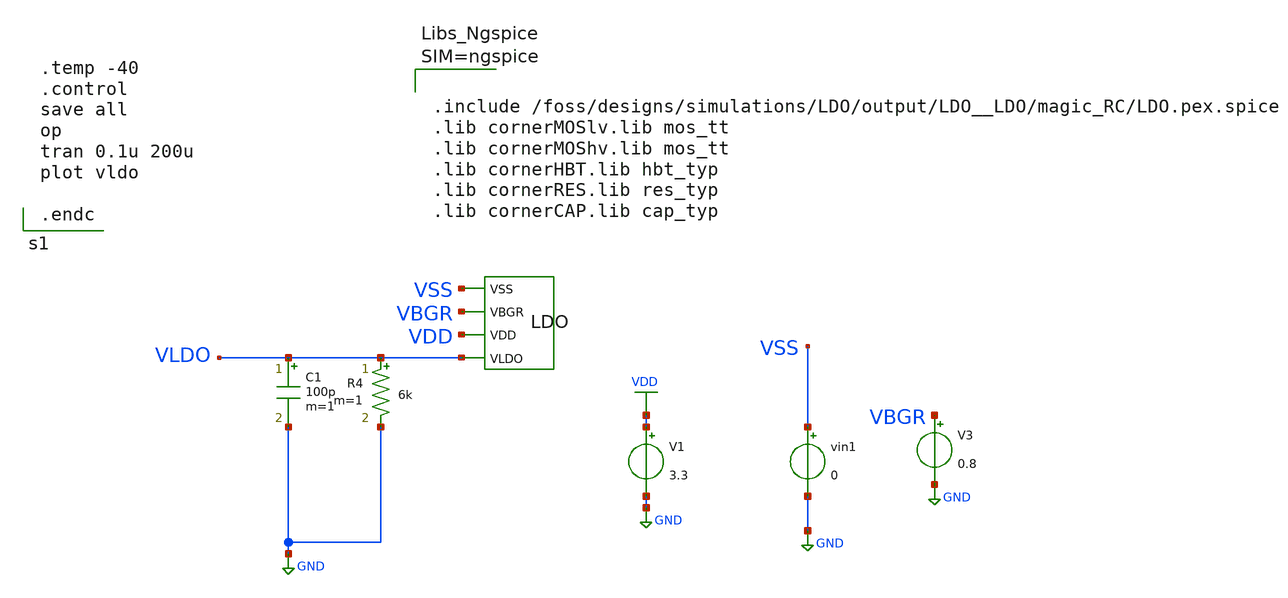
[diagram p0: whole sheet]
** sch_path: dependencies/LDO/LDO-main/testbenches/corners/xschem/ldo_post_layout_sim_tt_m40C.sch
**.subckt ldo_post_layout_sim_tt_m40C
V3 VBGR GND 0.8
vin1 VSS GND 0
V1 VDD GND 3.3
X1 VSS VBGR VDD VLDO LDO
C1 VLDO GND 100p m=1
R4 VLDO GND 6k m=1
**** begin user architecture code



.include /foss/designs/simulations/LDO/output/LDO__LDO/magic_RC/LDO.pex.spice
.lib cornerMOSlv.lib mos_tt
.lib cornerMOShv.lib mos_tt
.lib cornerHBT.lib hbt_typ
.lib cornerRES.lib res_typ
.lib cornerCAP.lib cap_typ





.temp -40
.control
save all
op
tran 0.1u 200u
plot vldo

.endc

**** end user architecture code
**.ends
.GLOBAL GND
.GLOBAL VDD
.end
